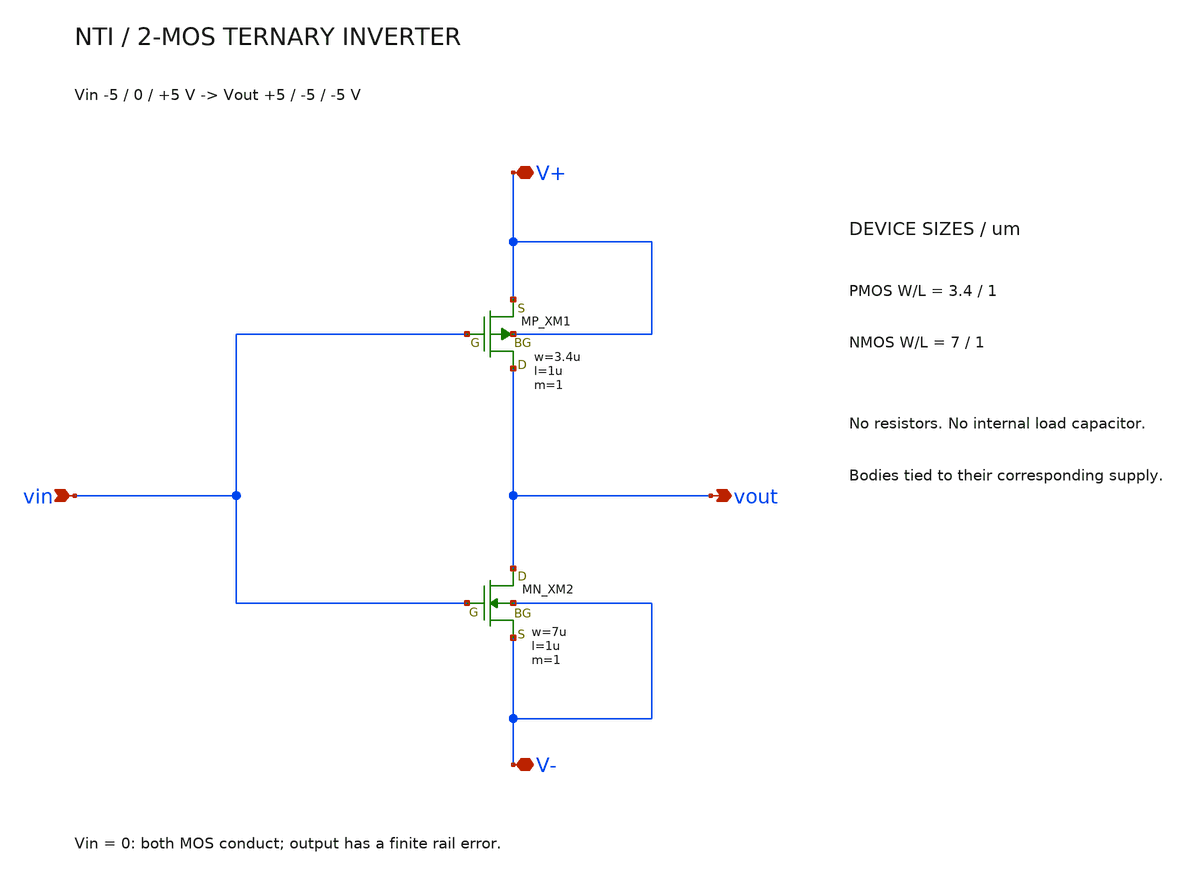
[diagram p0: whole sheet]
** sch_path: member_project/balanced-ternary-logic/PenguinEino/nti.sch
**.subckt nti V+ vout vin V-
*.iopin V+
*.opin vout
*.ipin vin
*.iopin V-
XXM1 vout vin V+ V+ PMOS w=3.4u l=1u nrd=0 nrs=0 m=1
XXM2 vout vin V- V- NMOS w=7u l=1u nrd=0 nrs=0 m=1
**.ends
.end
